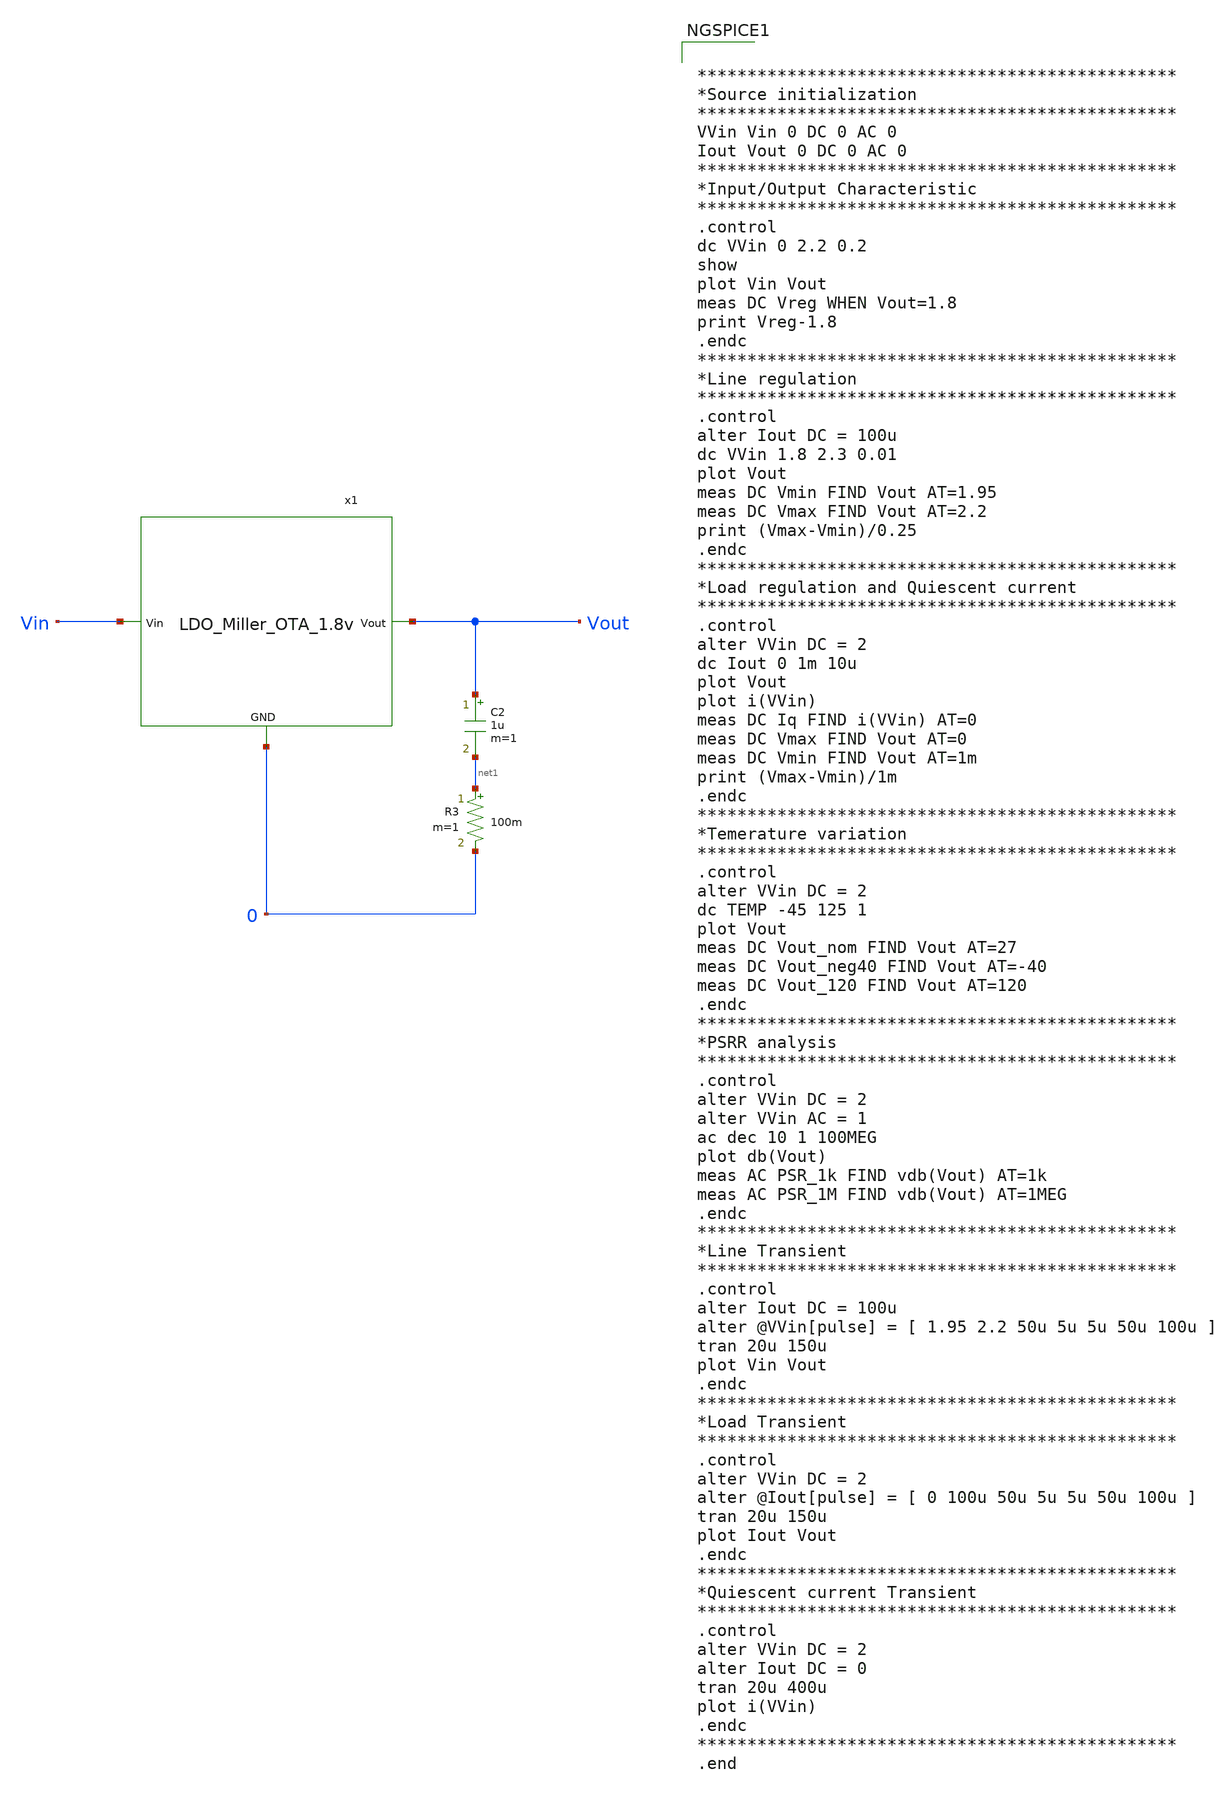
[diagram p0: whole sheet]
** sch_path: xschem/LDO_Miller_1.8v_meas.sch
**.subckt LDO_Miller_1.8v_meas
C2 Vout net1 1u m=1
R3 net1 0 100m m=1
x1 Vin Vout 0 LDO_Miller_OTA_1.8v
**** begin user architecture code


************************************************
*Source initialization
************************************************
VVin Vin 0 DC 0 AC 0
Iout Vout 0 DC 0 AC 0
************************************************
*Input/Output Characteristic
************************************************
.control
dc VVin 0 2.2 0.2
show
plot Vin Vout
meas DC Vreg WHEN Vout=1.8
print Vreg-1.8
.endc
************************************************
*Line regulation
************************************************
.control
alter Iout DC = 100u
dc VVin 1.8 2.3 0.01
plot Vout
meas DC Vmin FIND Vout AT=1.95
meas DC Vmax FIND Vout AT=2.2
print (Vmax-Vmin)/0.25
.endc
************************************************
*Load regulation and Quiescent current
************************************************
.control
alter VVin DC = 2
dc Iout 0 1m 10u
plot Vout
plot i(VVin)
meas DC Iq FIND i(VVin) AT=0
meas DC Vmax FIND Vout AT=0
meas DC Vmin FIND Vout AT=1m
print (Vmax-Vmin)/1m
.endc
************************************************
*Temerature variation
************************************************
.control
alter VVin DC = 2
dc TEMP -45 125 1
plot Vout
meas DC Vout_nom FIND Vout AT=27
meas DC Vout_neg40 FIND Vout AT=-40
meas DC Vout_120 FIND Vout AT=120
.endc
************************************************
*PSRR analysis
************************************************
.control
alter VVin DC = 2
alter VVin AC = 1
ac dec 10 1 100MEG
plot db(Vout)
meas AC PSR_1k FIND vdb(Vout) AT=1k
meas AC PSR_1M FIND vdb(Vout) AT=1MEG
.endc
************************************************
*Line Transient
************************************************
.control
alter Iout DC = 100u
alter @VVin[pulse] = [ 1.95 2.2 50u 5u 5u 50u 100u ]
tran 20u 150u
plot Vin Vout
.endc
************************************************
*Load Transient
************************************************
.control
alter VVin DC = 2
alter @Iout[pulse] = [ 0 100u 50u 5u 5u 50u 100u ]
tran 20u 150u
plot Iout Vout
.endc
************************************************
*Quiescent current Transient
************************************************
.control
alter VVin DC = 2
alter Iout DC = 0
tran 20u 400u
plot i(VVin)
.endc
************************************************
.end



.lib /home/designer/.volare/sky130A/libs.tech/ngspice/sky130.lib.spice tt
.include /home/designer/.volare/sky130A/libs.ref/sky130_fd_pr/spice/sky130_fd_pr__cap_mim_m3_2.model.spice

**** end user architecture code
**.ends
.end
